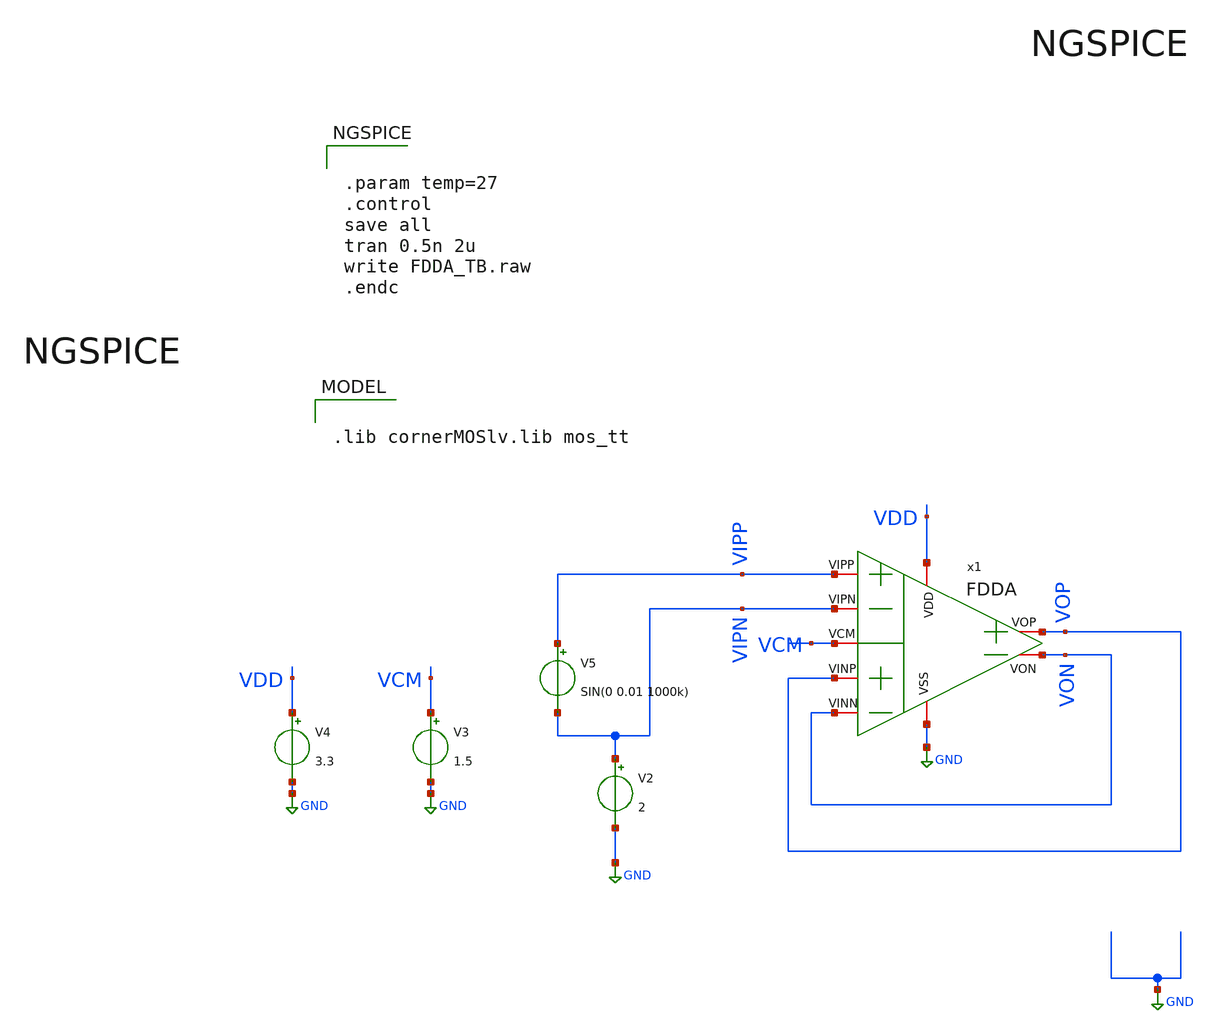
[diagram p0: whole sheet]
** sch_path: readout_circuit/analog/INA/FDDA/testbench/FDDA_TB.sch
**.subckt FDDA_TB
V2 VIPN GND 2
V3 VCM GND 1.5
V4 VDD GND 3.3
V5 VIPP VIPN SIN(0 0.01 1000k)
x1 VDD VIPN VCM VIPP VOP VON VOP VON GND FDDA
**** begin user architecture code

.lib cornerMOSlv.lib mos_tt



.param temp=27
.control
save all
tran 0.5n 2u
write FDDA_TB.raw
.endc


**** end user architecture code
**.ends

* expanding   symbol:  /home/designer/shared/readout_circuit/analog/INA/FDDA/schematic/FDDA.sym # of
*+ pins=9
** sym_path: readout_circuit/analog/INA/FDDA/schematic/FDDA.sym
** sch_path: readout_circuit/analog/INA/FDDA/schematic/FDDA.sch
.subckt FDDA VDD VIPN VCM VIPP VOP VINN VINP VON VSS
*.iopin VDD
*.iopin VSS
*.iopin VOP
*.iopin VON
*.iopin VIPP
*.iopin VINN
*.iopin VIPN
*.iopin VINP
*.iopin VCM
XM3 VON VB3 net5 VSS sg13_lv_nmos w=2u l=2u ng=4 m=80 mm_ok=1
XM4 VOP VB3 net4 VSS sg13_lv_nmos w=2u l=2u ng=4 m=80 mm_ok=1
XM5 VON VB4 net2 VDD sg13_lv_pmos w=3.5u l=2u ng=4 m=64 mm_ok=1
XM6 VOP VB4 net1 VDD sg13_lv_pmos w=3.5u l=2u ng=4 m=64 mm_ok=1
XM7 net2 VB1 VDD VDD sg13_lv_pmos w=3.5u l=2u ng=4 m=128 mm_ok=1
XM8 net1 VB1 VDD VDD sg13_lv_pmos w=3.5u l=2u ng=4 m=128 mm_ok=1
XM9 net4 VIPN net3 VDD sg13_lv_pmos w=3.5u l=2u ng=2 m=24 mm_ok=1
XM10 net5 VIPP net3 VDD sg13_lv_pmos w=3.5u l=2u ng=2 m=24 mm_ok=1
XM11 net3 VB1 VDD VDD sg13_lv_pmos w=3.5u l=2u ng=4 m=128 mm_ok=1
XM12 net4 VINP net6 VDD sg13_lv_pmos w=3.5u l=2u ng=2 m=24 mm_ok=1
XM13 net5 VINN net6 VDD sg13_lv_pmos w=3.5u l=2u ng=2 m=24 mm_ok=1
XM14 net6 VB1 VDD VDD sg13_lv_pmos w=3.5u l=2u ng=4 m=128 mm_ok=1
XM15 net10 VON net7 VDD sg13_lv_pmos w=2u l=2u ng=1 m=8 mm_ok=1
XM16 CMFB VCM net7 VDD sg13_lv_pmos w=2u l=2u ng=1 m=8 mm_ok=1
XM17 net7 VB1 VDD VDD sg13_lv_pmos w=3.5u l=2u ng=4 m=8 mm_ok=1
XM18 CMFB VCM net8 VDD sg13_lv_pmos w=2u l=2u ng=1 m=8 mm_ok=1
XM19 net9 VOP net8 VDD sg13_lv_pmos w=2u l=2u ng=1 m=8 mm_ok=1
XM20 net8 VB1 VDD VDD sg13_lv_pmos w=3.5u l=2u ng=4 m=8 mm_ok=1
XM21 net10 net10 VSS VSS sg13_lv_nmos w=2u l=2u ng=1 m=2 mm_ok=1
XM22 net9 net9 VSS VSS sg13_lv_nmos w=2u l=2u ng=1 m=2 mm_ok=1
XM23 CMFB net10 VSS VSS sg13_lv_nmos w=2u l=2u ng=1 m=2 mm_ok=1
XM24 net5 CMFB VSS VSS sg13_lv_nmos w=2u l=2u ng=4 m=256 mm_ok=1
XM25 net4 CMFB VSS VSS sg13_lv_nmos w=2u l=2u ng=4 m=256 mm_ok=1
XM26 VB2 VB2 VSS VSS sg13_lv_nmos w=2u l=2u ng=4 m=16 mm_ok=1
XM27 VB3 VB3 VSS VSS sg13_lv_nmos w=2u l=2u ng=1 m=1 mm_ok=1
XM28 VB1 VB1 VDD VDD sg13_lv_pmos w=3.5u l=2u ng=4 m=16 mm_ok=1
XM29 VB4 VB4 VDD VDD sg13_lv_pmos w=3.5u l=2u ng=2 m=1 mm_ok=1
I0 VB1 VSS 20u
I1 VB4 VSS 20u
I2 VDD VB3 20u
I3 VDD VB2 20u
XM1 CMFB net9 VSS VSS sg13_lv_nmos w=2u l=2u ng=1 m=2 mm_ok=1
C1 CMFB VSS 200p m=1
.ends

.GLOBAL GND
.end
